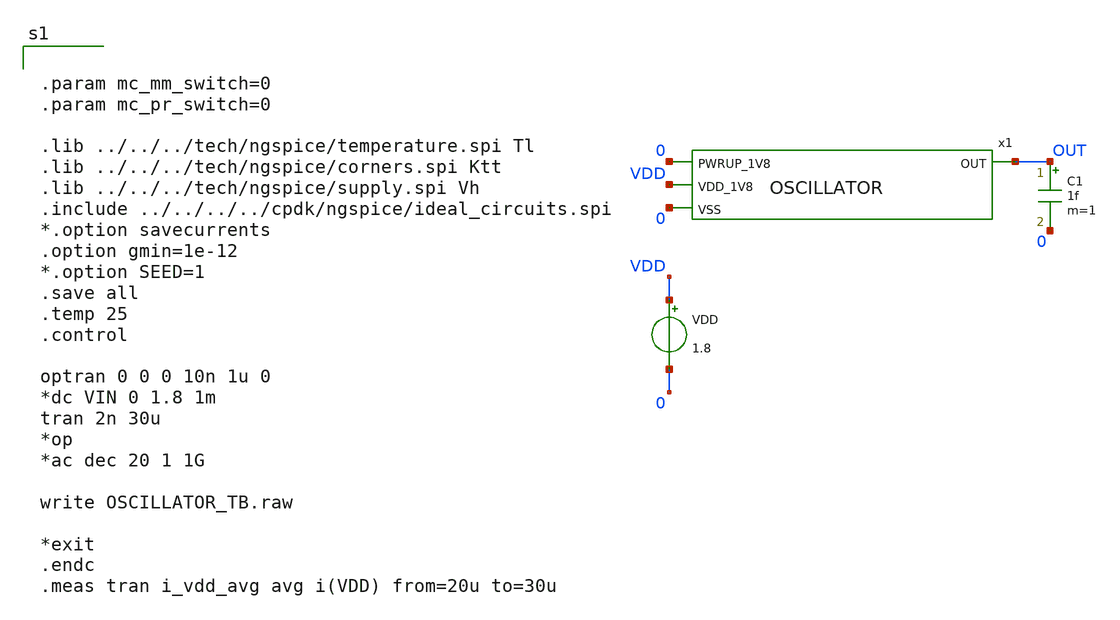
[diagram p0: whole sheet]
** sch_path: design/LELO_GR03_SKY130A/OSCILLATOR_TB_xsch.sch
**.subckt OSCILLATOR_TB_xsch
x1 0 OUT VDD 0 OSCILLATOR
VDD VDD 0 1.8
C1 OUT 0 1f m=1
**** begin user architecture code


.param mc_mm_switch=0
.param mc_pr_switch=0

.lib ../../../tech/ngspice/temperature.spi Tl
.lib ../../../tech/ngspice/corners.spi Ktt
.lib ../../../tech/ngspice/supply.spi Vh
.include ../../../../cpdk/ngspice/ideal_circuits.spi
*.option savecurrents
.option gmin=1e-12
*.option SEED=1
.save all
.temp 25
.control

optran 0 0 0 10n 1u 0
*dc VIN 0 1.8 1m
tran 2n 30u
*op
*ac dec 20 1 1G

write OSCILLATOR_TB.raw

*exit
.endc
.meas tran i_vdd_avg avg i(VDD) from=20u to=30u


**** end user architecture code
**.ends
.end
